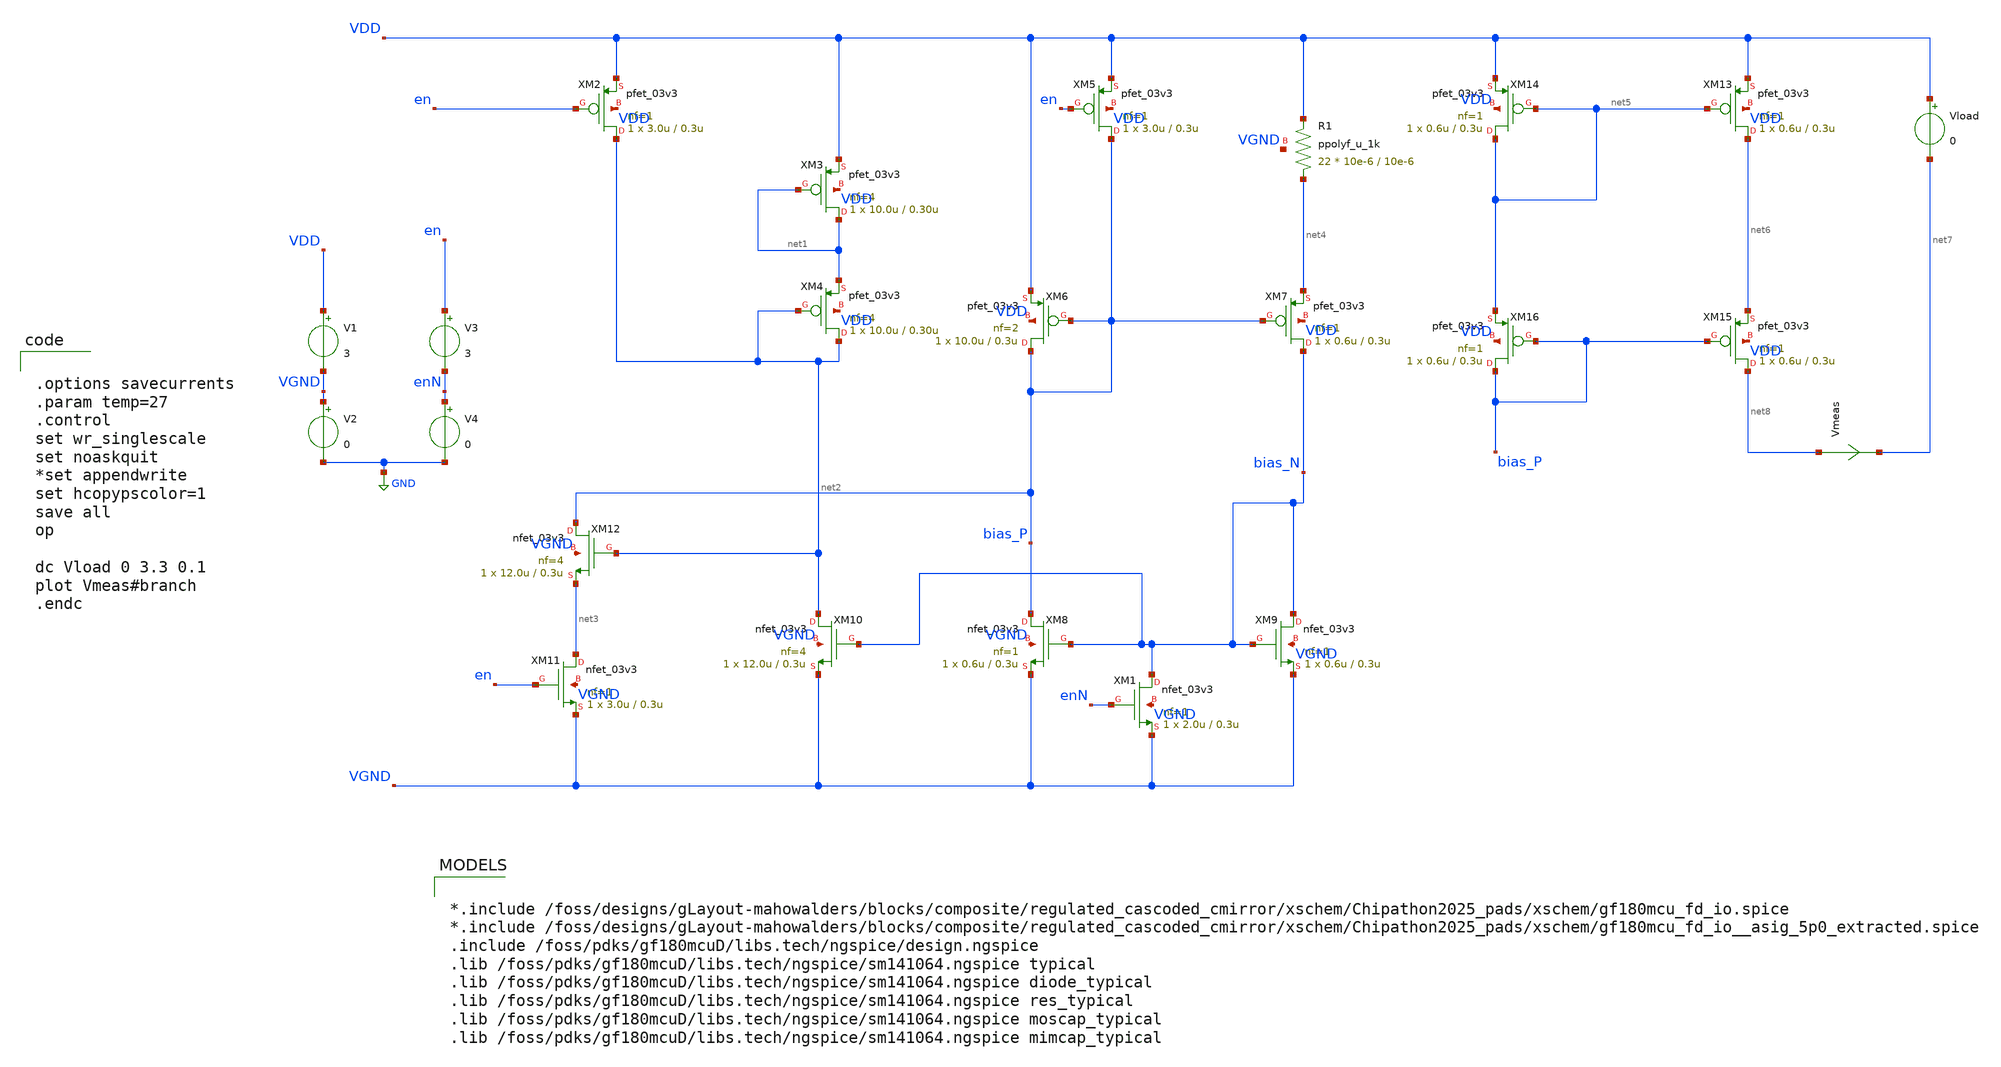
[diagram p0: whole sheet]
** sch_path: blocks/composite/regulated_cascoded_cmirror/xschem/bias_INT.sch
**.subckt bias_INT
XM2 net2 en VDD VDD pfet_03v3 L=0.3u W=3.0u nf=1 ad='int((nf+1)/2) * W/nf * 0.18u' as='int((nf+2)/2) * W/nf * 0.18u'
+ pd='2*int((nf+1)/2) * (W/nf + 0.18u)' ps='2*int((nf+2)/2) * (W/nf + 0.18u)' nrd='0.18u / W' nrs='0.18u / W'
+ sa=0 sb=0 sd=0 m=1
XM3 net1 net1 VDD VDD pfet_03v3 L=0.30u W=10.0u nf=4 ad='int((nf+1)/2) * W/nf * 0.18u' as='int((nf+2)/2) * W/nf * 0.18u'
+ pd='2*int((nf+1)/2) * (W/nf + 0.18u)' ps='2*int((nf+2)/2) * (W/nf + 0.18u)' nrd='0.18u / W' nrs='0.18u / W'
+ sa=0 sb=0 sd=0 m=1
XM4 net2 net2 net1 VDD pfet_03v3 L=0.30u W=10.0u nf=4 ad='int((nf+1)/2) * W/nf * 0.18u' as='int((nf+2)/2) * W/nf * 0.18u'
+ pd='2*int((nf+1)/2) * (W/nf + 0.18u)' ps='2*int((nf+2)/2) * (W/nf + 0.18u)' nrd='0.18u / W' nrs='0.18u / W'
+ sa=0 sb=0 sd=0 m=1
XM5 bias_P en VDD VDD pfet_03v3 L=0.3u W=3.0u nf=1 ad='int((nf+1)/2) * W/nf * 0.18u' as='int((nf+2)/2) * W/nf * 0.18u'
+ pd='2*int((nf+1)/2) * (W/nf + 0.18u)' ps='2*int((nf+2)/2) * (W/nf + 0.18u)' nrd='0.18u / W' nrs='0.18u / W'
+ sa=0 sb=0 sd=0 m=1
XM6 bias_P bias_P VDD VDD pfet_03v3 L=0.3u W=10.0u nf=2 ad='int((nf+1)/2) * W/nf * 0.18u' as='int((nf+2)/2) * W/nf * 0.18u'
+ pd='2*int((nf+1)/2) * (W/nf + 0.18u)' ps='2*int((nf+2)/2) * (W/nf + 0.18u)' nrd='0.18u / W' nrs='0.18u / W'
+ sa=0 sb=0 sd=0 m=1
XM7 bias_N bias_P net4 VDD pfet_03v3 L=0.3u W=0.6u nf=1 ad='int((nf+1)/2) * W/nf * 0.18u' as='int((nf+2)/2) * W/nf * 0.18u'
+ pd='2*int((nf+1)/2) * (W/nf + 0.18u)' ps='2*int((nf+2)/2) * (W/nf + 0.18u)' nrd='0.18u / W' nrs='0.18u / W'
+ sa=0 sb=0 sd=0 m=1
XM8 bias_P bias_N VGND VGND nfet_03v3 L=0.3u W=0.6u nf=1 ad='int((nf+1)/2) * W/nf * 0.18u' as='int((nf+2)/2) * W/nf * 0.18u'
+ pd='2*int((nf+1)/2) * (W/nf + 0.18u)' ps='2*int((nf+2)/2) * (W/nf + 0.18u)' nrd='0.18u / W' nrs='0.18u / W'
+ sa=0 sb=0 sd=0 m=1
XM9 bias_N bias_N VGND VGND nfet_03v3 L=0.3u W=0.6u nf=1 ad='int((nf+1)/2) * W/nf * 0.18u' as='int((nf+2)/2) * W/nf * 0.18u'
+ pd='2*int((nf+1)/2) * (W/nf + 0.18u)' ps='2*int((nf+2)/2) * (W/nf + 0.18u)' nrd='0.18u / W' nrs='0.18u / W'
+ sa=0 sb=0 sd=0 m=1
XM1 bias_N enN VGND VGND nfet_03v3 L=0.3u W=2.0u nf=1 ad='int((nf+1)/2) * W/nf * 0.18u' as='int((nf+2)/2) * W/nf * 0.18u'
+ pd='2*int((nf+1)/2) * (W/nf + 0.18u)' ps='2*int((nf+2)/2) * (W/nf + 0.18u)' nrd='0.18u / W' nrs='0.18u / W'
+ sa=0 sb=0 sd=0 m=1
XM10 net2 bias_N VGND VGND nfet_03v3 L=0.3u W=12.0u nf=4 ad='int((nf+1)/2) * W/nf * 0.18u' as='int((nf+2)/2) * W/nf * 0.18u'
+ pd='2*int((nf+1)/2) * (W/nf + 0.18u)' ps='2*int((nf+2)/2) * (W/nf + 0.18u)' nrd='0.18u / W' nrs='0.18u / W'
+ sa=0 sb=0 sd=0 m=1
XM11 net3 en VGND VGND nfet_03v3 L=0.3u W=3.0u nf=1 ad='int((nf+1)/2) * W/nf * 0.18u' as='int((nf+2)/2) * W/nf * 0.18u'
+ pd='2*int((nf+1)/2) * (W/nf + 0.18u)' ps='2*int((nf+2)/2) * (W/nf + 0.18u)' nrd='0.18u / W' nrs='0.18u / W'
+ sa=0 sb=0 sd=0 m=1
XM12 bias_P net2 net3 VGND nfet_03v3 L=0.3u W=12.0u nf=4 ad='int((nf+1)/2) * W/nf * 0.18u' as='int((nf+2)/2) * W/nf * 0.18u'
+ pd='2*int((nf+1)/2) * (W/nf + 0.18u)' ps='2*int((nf+2)/2) * (W/nf + 0.18u)' nrd='0.18u / W' nrs='0.18u / W'
+ sa=0 sb=0 sd=0 m=1
XR1 net4 VDD VGND ppolyf_u_1k r_width=10e-6 r_length=10e-6 m=22
V1 VDD VGND 3
V2 VGND GND 0
V3 en enN 3
V4 enN GND 0
XM13 net6 net5 VDD VDD pfet_03v3 L=0.3u W=0.6u nf=1 ad='int((nf+1)/2) * W/nf * 0.18u' as='int((nf+2)/2) * W/nf * 0.18u'
+ pd='2*int((nf+1)/2) * (W/nf + 0.18u)' ps='2*int((nf+2)/2) * (W/nf + 0.18u)' nrd='0.18u / W' nrs='0.18u / W'
+ sa=0 sb=0 sd=0 m=1
XM14 net5 net5 VDD VDD pfet_03v3 L=0.3u W=0.6u nf=1 ad='int((nf+1)/2) * W/nf * 0.18u' as='int((nf+2)/2) * W/nf * 0.18u'
+ pd='2*int((nf+1)/2) * (W/nf + 0.18u)' ps='2*int((nf+2)/2) * (W/nf + 0.18u)' nrd='0.18u / W' nrs='0.18u / W'
+ sa=0 sb=0 sd=0 m=1
Vload VDD net7 0
Vmeas net8 net7 0
.save i(vmeas)
XM15 net8 bias_P net6 VDD pfet_03v3 L=0.3u W=0.6u nf=1 ad='int((nf+1)/2) * W/nf * 0.18u' as='int((nf+2)/2) * W/nf * 0.18u'
+ pd='2*int((nf+1)/2) * (W/nf + 0.18u)' ps='2*int((nf+2)/2) * (W/nf + 0.18u)' nrd='0.18u / W' nrs='0.18u / W'
+ sa=0 sb=0 sd=0 m=1
XM16 bias_P bias_P net5 VDD pfet_03v3 L=0.3u W=0.6u nf=1 ad='int((nf+1)/2) * W/nf * 0.18u' as='int((nf+2)/2) * W/nf * 0.18u'
+ pd='2*int((nf+1)/2) * (W/nf + 0.18u)' ps='2*int((nf+2)/2) * (W/nf + 0.18u)' nrd='0.18u / W' nrs='0.18u / W'
+ sa=0 sb=0 sd=0 m=1
**** begin user architecture code

*.include /foss/designs/gLayout-mahowalders/blocks/composite/regulated_cascoded_cmirror/xschem/Chipathon2025_pads/xschem/gf180mcu_fd_io.spice
*.include /foss/designs/gLayout-mahowalders/blocks/composite/regulated_cascoded_cmirror/xschem/Chipathon2025_pads/xschem/gf180mcu_fd_io__asig_5p0_extracted.spice
.include /foss/pdks/gf180mcuD/libs.tech/ngspice/design.ngspice
.lib /foss/pdks/gf180mcuD/libs.tech/ngspice/sm141064.ngspice typical
.lib /foss/pdks/gf180mcuD/libs.tech/ngspice/sm141064.ngspice diode_typical
.lib /foss/pdks/gf180mcuD/libs.tech/ngspice/sm141064.ngspice res_typical
.lib /foss/pdks/gf180mcuD/libs.tech/ngspice/sm141064.ngspice moscap_typical
.lib /foss/pdks/gf180mcuD/libs.tech/ngspice/sm141064.ngspice mimcap_typical



.options savecurrents
.param temp=27
.control
set wr_singlescale
set noaskquit
*set appendwrite
set hcopypscolor=1
save all
op

dc Vload 0 3.3 0.1
plot Vmeas#branch
.endc



**** end user architecture code
**.ends
.GLOBAL GND
.end
